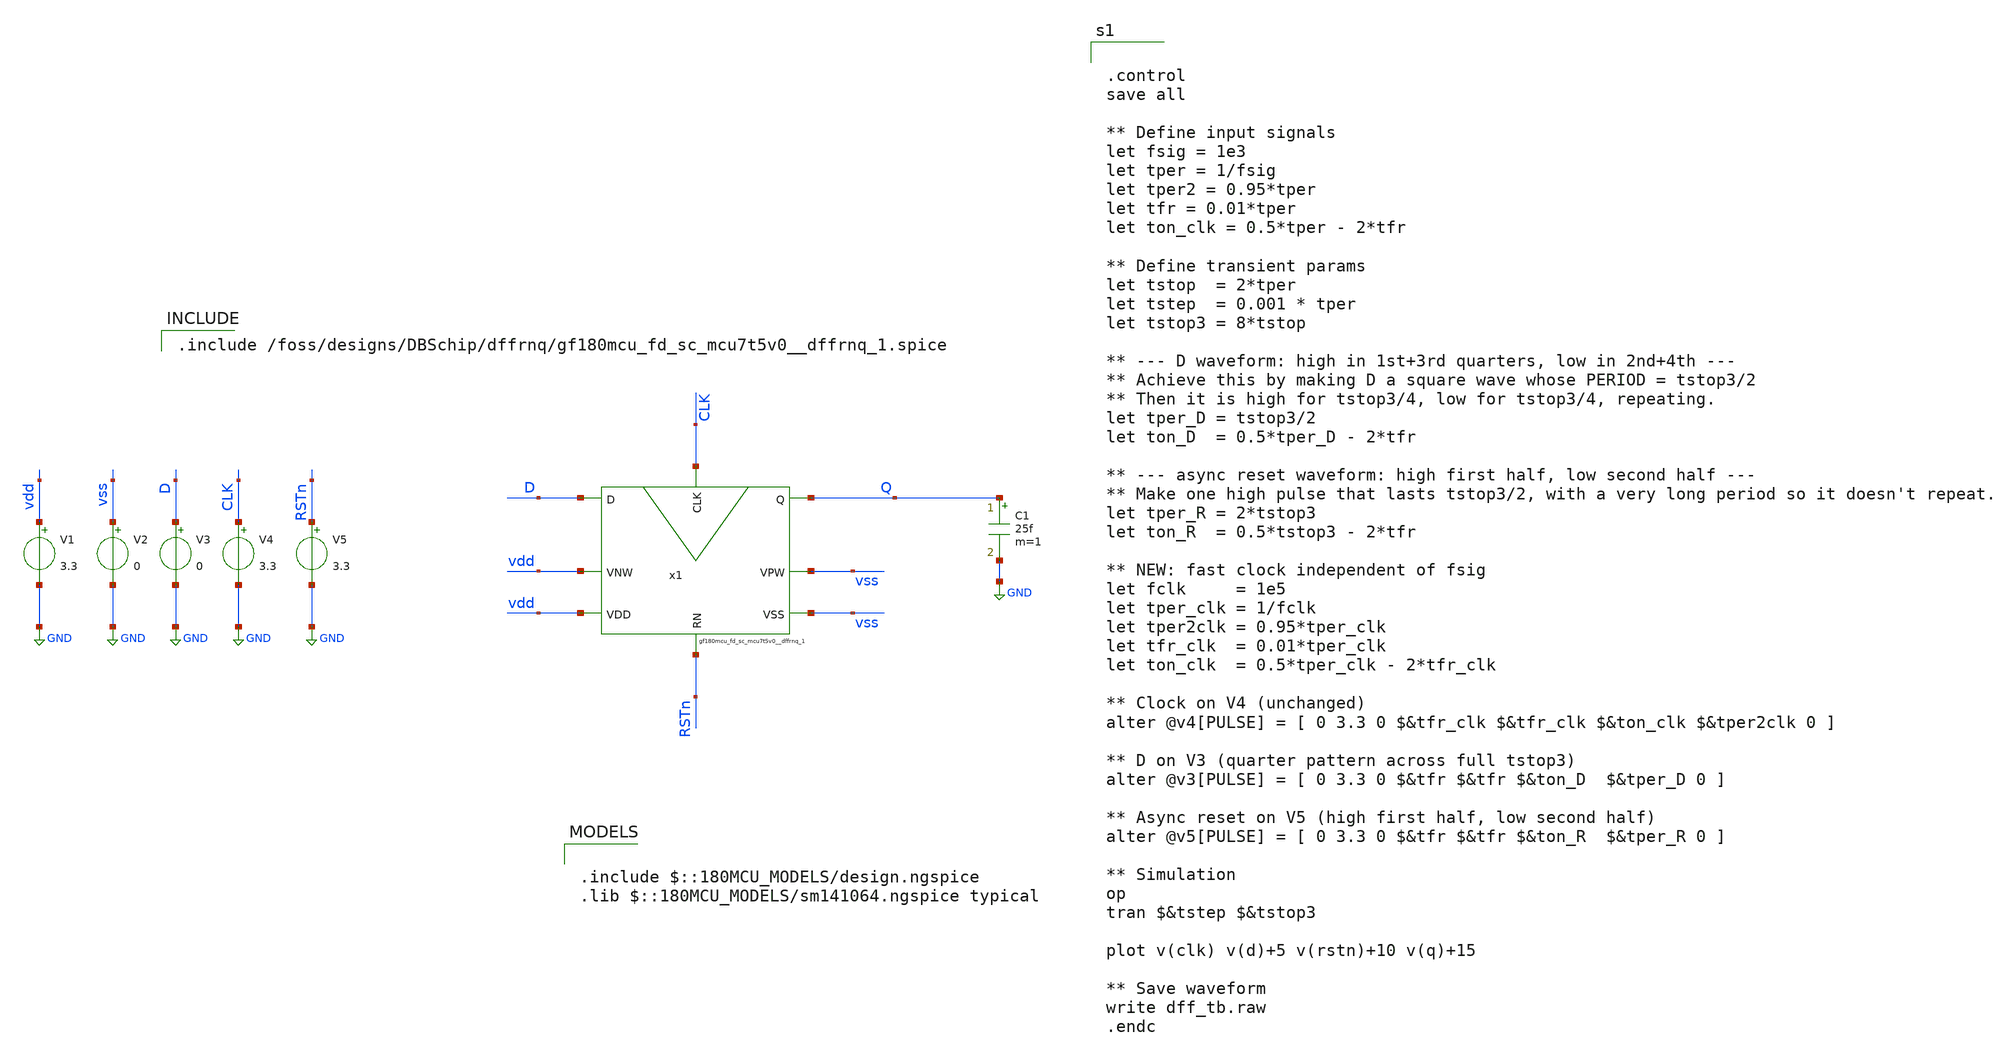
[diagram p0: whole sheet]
** sch_path: dffrnq/dffrnq_tb.sch
**.subckt dffrnq_tb
x1 D RSTn CLK Q vdd vdd vss vss gf180mcu_fd_sc_mcu7t5v0__dffrnq_1
V1 vdd GND 3.3
V2 vss GND 0
V3 D GND 0
V4 CLK GND 3.3
V5 RSTn GND 3.3
C1 Q GND 25f m=1
**** begin user architecture code

.include /foss/designs/DBSchip/dffrnq/gf180mcu_fd_sc_mcu7t5v0__dffrnq_1.spice



.control
save all

** Define input signals
let fsig = 1e3
let tper = 1/fsig
let tper2 = 0.95*tper
let tfr = 0.01*tper
let ton_clk = 0.5*tper - 2*tfr

** Define transient params
let tstop  = 2*tper
let tstep  = 0.001 * tper
let tstop3 = 8*tstop

** --- D waveform: high in 1st+3rd quarters, low in 2nd+4th ---
** Achieve this by making D a square wave whose PERIOD = tstop3/2
** Then it is high for tstop3/4, low for tstop3/4, repeating.
let tper_D = tstop3/2
let ton_D  = 0.5*tper_D - 2*tfr

** --- async reset waveform: high first half, low second half ---
** Make one high pulse that lasts tstop3/2, with a very long period so it doesn't repeat.
let tper_R = 2*tstop3
let ton_R  = 0.5*tstop3 - 2*tfr

** NEW: fast clock independent of fsig
let fclk     = 1e5
let tper_clk = 1/fclk
let tper2clk = 0.95*tper_clk
let tfr_clk  = 0.01*tper_clk
let ton_clk  = 0.5*tper_clk - 2*tfr_clk

** Clock on V4 (unchanged)
alter @v4[PULSE] = [ 0 3.3 0 $&tfr_clk $&tfr_clk $&ton_clk $&tper2clk 0 ]

** D on V3 (quarter pattern across full tstop3)
alter @v3[PULSE] = [ 0 3.3 0 $&tfr $&tfr $&ton_D  $&tper_D 0 ]

** Async reset on V5 (high first half, low second half)
alter @v5[PULSE] = [ 0 3.3 0 $&tfr $&tfr $&ton_R  $&tper_R 0 ]

** Simulation
op
tran $&tstep $&tstop3

plot v(clk) v(d)+5 v(rstn)+10 v(q)+15

** Save waveform
write dff_tb.raw
.endc






.include $::180MCU_MODELS/design.ngspice
.lib $::180MCU_MODELS/sm141064.ngspice typical

**** end user architecture code
**.ends
.GLOBAL GND
.end
